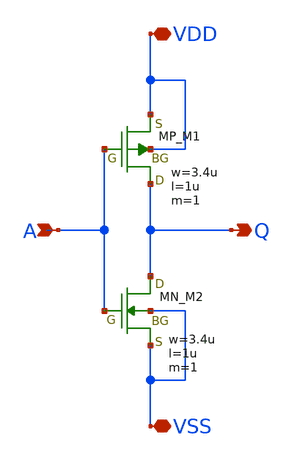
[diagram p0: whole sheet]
** sch_path: member_project/ringOSC/noritsuna/inverter_kato1.sch
**.subckt inverter_kato1 A Q VSS VDD
*.ipin A
*.opin Q
*.iopin VSS
*.iopin VDD
XM1 Q A VDD VDD PMOS w=3.4u l=1u nrd=0 nrs=0 m=1
XM2 Q A VSS VSS NMOS w=3.4u l=1u nrd=0 nrs=0 m=1
**.ends
.end
